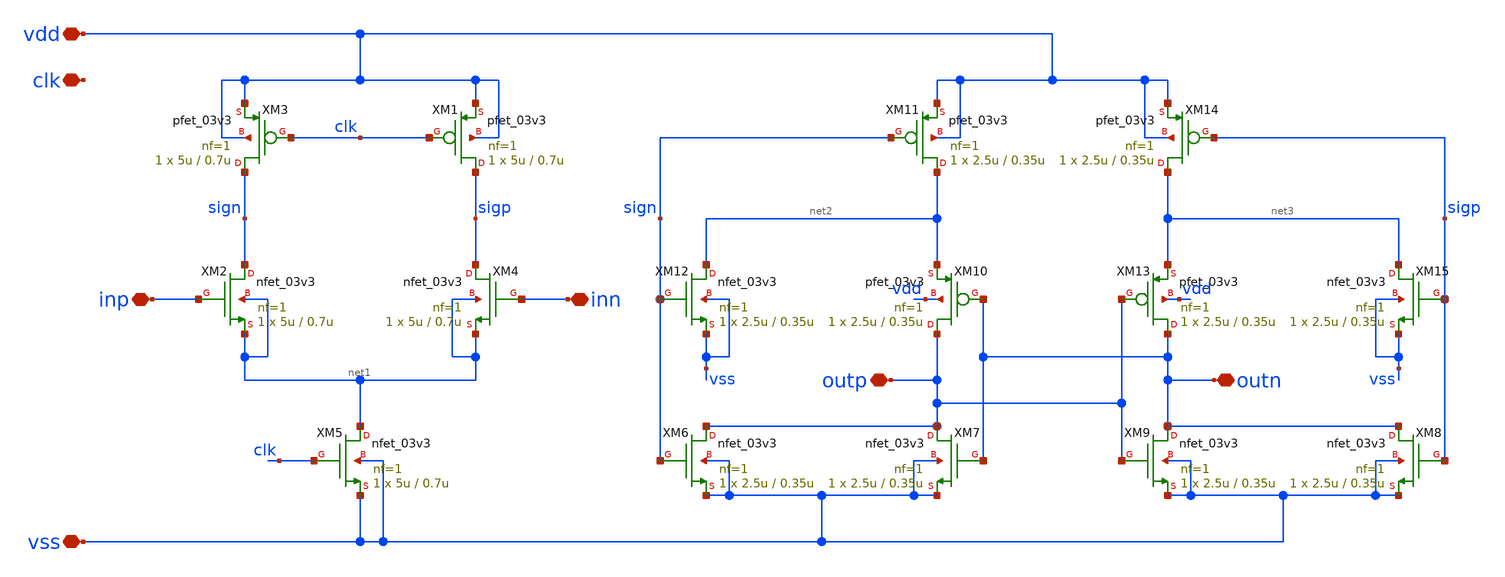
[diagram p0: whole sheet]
** sch_path: designs/libs/qw_core_analog_pkedit/Comparator_doubletail.sch
**.subckt Comparator_doubletail vdd vss clk inp inn outp outn
*.iopin vdd
*.iopin vss
*.iopin clk
*.iopin inp
*.iopin inn
*.iopin outp
*.iopin outn
XM1 sigp clk vdd vdd pfet_03v3 L=0.7u W=5u nf=1 ad='int((nf+1)/2) * W/nf * 0.18u' as='int((nf+2)/2) * W/nf * 0.18u'
+ pd='2*int((nf+1)/2) * (W/nf + 0.18u)' ps='2*int((nf+2)/2) * (W/nf + 0.18u)' nrd='0.18u / W' nrs='0.18u / W'
+ sa=0 sb=0 sd=0 m=1
XM2 sign inp net1 net1 nfet_03v3 L=0.7u W=5u nf=1 ad='int((nf+1)/2) * W/nf * 0.18u' as='int((nf+2)/2) * W/nf * 0.18u'
+ pd='2*int((nf+1)/2) * (W/nf + 0.18u)' ps='2*int((nf+2)/2) * (W/nf + 0.18u)' nrd='0.18u / W' nrs='0.18u / W'
+ sa=0 sb=0 sd=0 m=1
XM3 sign clk vdd vdd pfet_03v3 L=0.7u W=5u nf=1 ad='int((nf+1)/2) * W/nf * 0.18u' as='int((nf+2)/2) * W/nf * 0.18u'
+ pd='2*int((nf+1)/2) * (W/nf + 0.18u)' ps='2*int((nf+2)/2) * (W/nf + 0.18u)' nrd='0.18u / W' nrs='0.18u / W'
+ sa=0 sb=0 sd=0 m=1
XM4 sigp inn net1 net1 nfet_03v3 L=0.7u W=5u nf=1 ad='int((nf+1)/2) * W/nf * 0.18u' as='int((nf+2)/2) * W/nf * 0.18u'
+ pd='2*int((nf+1)/2) * (W/nf + 0.18u)' ps='2*int((nf+2)/2) * (W/nf + 0.18u)' nrd='0.18u / W' nrs='0.18u / W'
+ sa=0 sb=0 sd=0 m=1
XM5 net1 clk vss vss nfet_03v3 L=0.7u W=5u nf=1 ad='int((nf+1)/2) * W/nf * 0.18u' as='int((nf+2)/2) * W/nf * 0.18u'
+ pd='2*int((nf+1)/2) * (W/nf + 0.18u)' ps='2*int((nf+2)/2) * (W/nf + 0.18u)' nrd='0.18u / W' nrs='0.18u / W'
+ sa=0 sb=0 sd=0 m=1
XM6 outp sign vss vss nfet_03v3 L=0.35u W=2.5u nf=1 ad='int((nf+1)/2) * W/nf * 0.18u' as='int((nf+2)/2) * W/nf * 0.18u'
+ pd='2*int((nf+1)/2) * (W/nf + 0.18u)' ps='2*int((nf+2)/2) * (W/nf + 0.18u)' nrd='0.18u / W' nrs='0.18u / W'
+ sa=0 sb=0 sd=0 m=1
XM7 outp outn vss vss nfet_03v3 L=0.35u W=2.5u nf=1 ad='int((nf+1)/2) * W/nf * 0.18u' as='int((nf+2)/2) * W/nf * 0.18u'
+ pd='2*int((nf+1)/2) * (W/nf + 0.18u)' ps='2*int((nf+2)/2) * (W/nf + 0.18u)' nrd='0.18u / W' nrs='0.18u / W'
+ sa=0 sb=0 sd=0 m=1
XM10 outp outn net2 vdd pfet_03v3 L=0.35u W=2.5u nf=1 ad='int((nf+1)/2) * W/nf * 0.18u' as='int((nf+2)/2) * W/nf * 0.18u'
+ pd='2*int((nf+1)/2) * (W/nf + 0.18u)' ps='2*int((nf+2)/2) * (W/nf + 0.18u)' nrd='0.18u / W' nrs='0.18u / W'
+ sa=0 sb=0 sd=0 m=1
XM11 net2 sign vdd vdd pfet_03v3 L=0.35u W=2.5u nf=1 ad='int((nf+1)/2) * W/nf * 0.18u' as='int((nf+2)/2) * W/nf * 0.18u'
+ pd='2*int((nf+1)/2) * (W/nf + 0.18u)' ps='2*int((nf+2)/2) * (W/nf + 0.18u)' nrd='0.18u / W' nrs='0.18u / W'
+ sa=0 sb=0 sd=0 m=1
XM12 net2 sign vss vss nfet_03v3 L=0.35u W=2.5u nf=1 ad='int((nf+1)/2) * W/nf * 0.18u' as='int((nf+2)/2) * W/nf * 0.18u'
+ pd='2*int((nf+1)/2) * (W/nf + 0.18u)' ps='2*int((nf+2)/2) * (W/nf + 0.18u)' nrd='0.18u / W' nrs='0.18u / W'
+ sa=0 sb=0 sd=0 m=1
XM8 outn sigp vss vss nfet_03v3 L=0.35u W=2.5u nf=1 ad='int((nf+1)/2) * W/nf * 0.18u' as='int((nf+2)/2) * W/nf * 0.18u'
+ pd='2*int((nf+1)/2) * (W/nf + 0.18u)' ps='2*int((nf+2)/2) * (W/nf + 0.18u)' nrd='0.18u / W' nrs='0.18u / W'
+ sa=0 sb=0 sd=0 m=1
XM9 outn outp vss vss nfet_03v3 L=0.35u W=2.5u nf=1 ad='int((nf+1)/2) * W/nf * 0.18u' as='int((nf+2)/2) * W/nf * 0.18u'
+ pd='2*int((nf+1)/2) * (W/nf + 0.18u)' ps='2*int((nf+2)/2) * (W/nf + 0.18u)' nrd='0.18u / W' nrs='0.18u / W'
+ sa=0 sb=0 sd=0 m=1
XM13 outn outp net3 vdd pfet_03v3 L=0.35u W=2.5u nf=1 ad='int((nf+1)/2) * W/nf * 0.18u' as='int((nf+2)/2) * W/nf * 0.18u'
+ pd='2*int((nf+1)/2) * (W/nf + 0.18u)' ps='2*int((nf+2)/2) * (W/nf + 0.18u)' nrd='0.18u / W' nrs='0.18u / W'
+ sa=0 sb=0 sd=0 m=1
XM14 net3 sigp vdd vdd pfet_03v3 L=0.35u W=2.5u nf=1 ad='int((nf+1)/2) * W/nf * 0.18u' as='int((nf+2)/2) * W/nf * 0.18u'
+ pd='2*int((nf+1)/2) * (W/nf + 0.18u)' ps='2*int((nf+2)/2) * (W/nf + 0.18u)' nrd='0.18u / W' nrs='0.18u / W'
+ sa=0 sb=0 sd=0 m=1
XM15 net3 sigp vss vss nfet_03v3 L=0.35u W=2.5u nf=1 ad='int((nf+1)/2) * W/nf * 0.18u' as='int((nf+2)/2) * W/nf * 0.18u'
+ pd='2*int((nf+1)/2) * (W/nf + 0.18u)' ps='2*int((nf+2)/2) * (W/nf + 0.18u)' nrd='0.18u / W' nrs='0.18u / W'
+ sa=0 sb=0 sd=0 m=1
**.ends
.end
